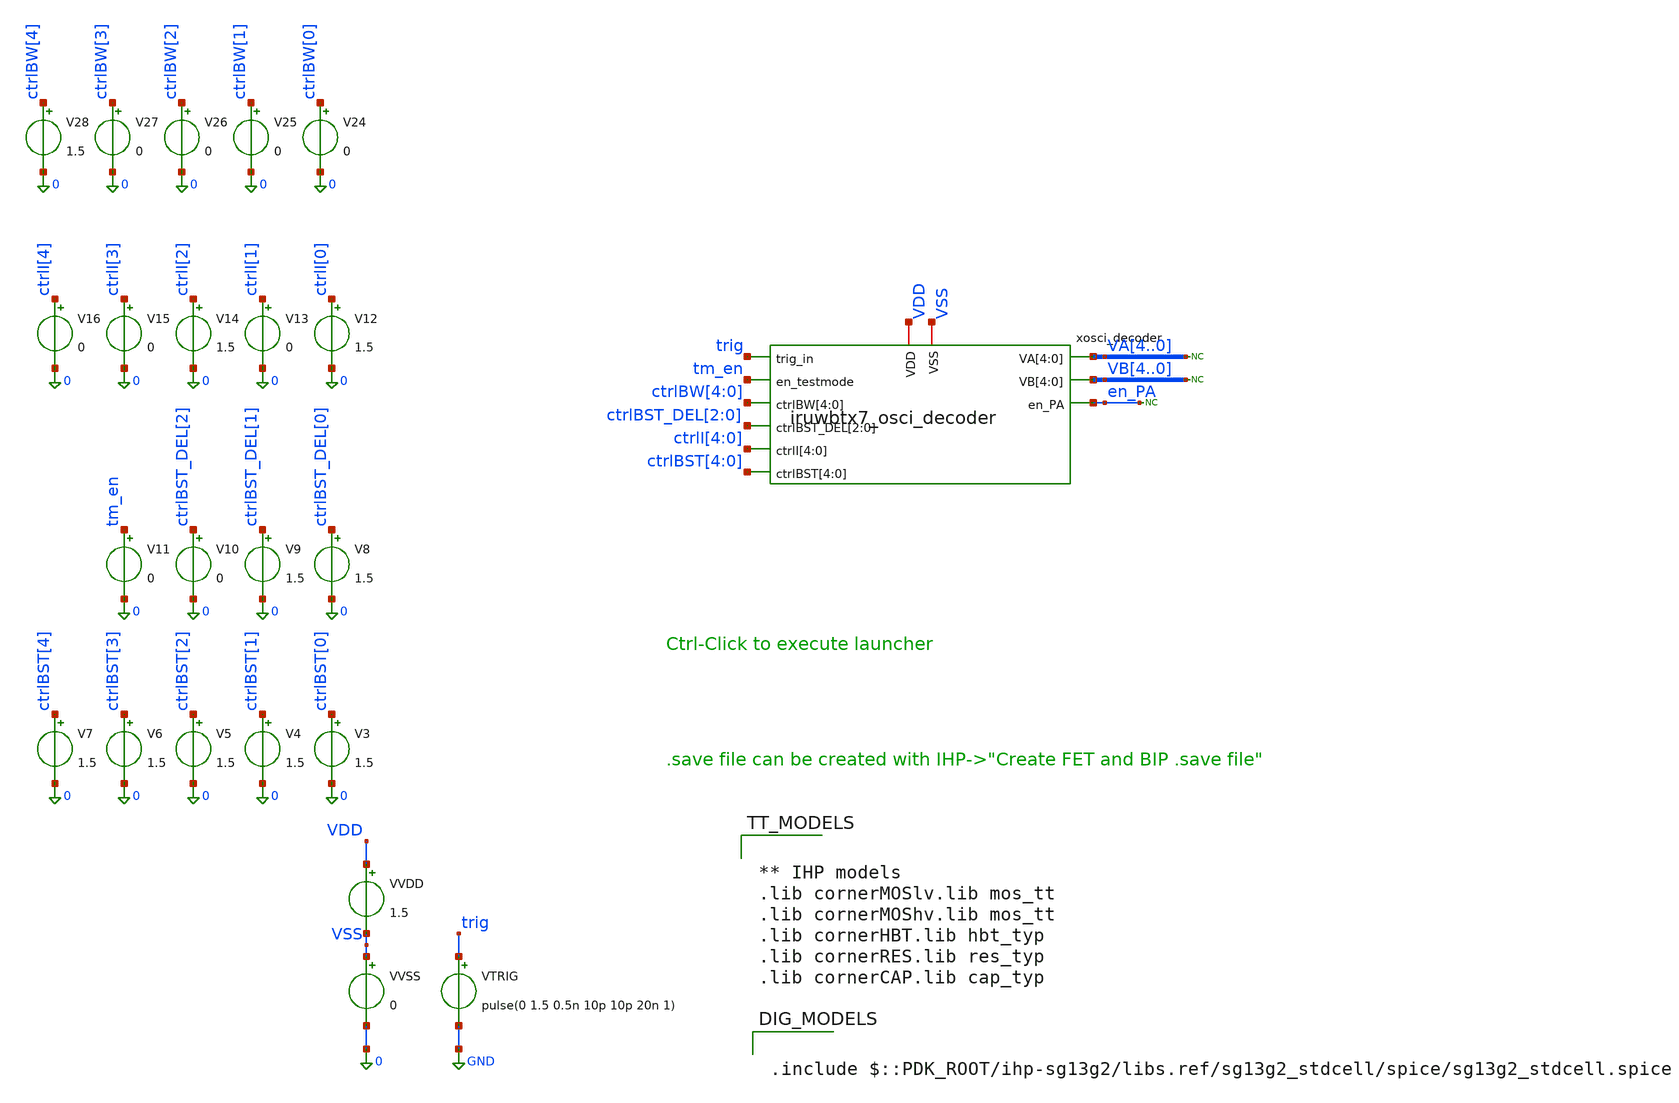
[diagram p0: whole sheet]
** sch_path: xschem/iruwbtx7_osci_decoder_tb.sch
* IHP-GmbH/IHP-Open-PDK/ihp-sg13g2/libs.tech/xschem/sg13g2_stdcells/sg13g2_inv_16.sch:
* Copyright 2023 IHP PDK Authors
* Licensed under the Apache License, Version 2.0 (the "License");
**.subckt iruwbtx7_osci_decoder_tb
VVDD VDD VSS 1.5
VVSS VSS 0 0
VTRIG trig GND pulse(0 1.5 0.5n 10p 10p 20n 1)
V3 ctrlBST[0] 0 1.5
V4 ctrlBST[1] 0 1.5
V5 ctrlBST[2] 0 1.5
V6 ctrlBST[3] 0 1.5
V7 ctrlBST[4] 0 1.5
V8 ctrlBST_DEL[0] 0 1.5
V9 ctrlBST_DEL[1] 0 1.5
V10 ctrlBST_DEL[2] 0 0
V11 tm_en 0 0
V12 ctrlI[0] 0 1.5
V13 ctrlI[1] 0 0
V14 ctrlI[2] 0 1.5
V15 ctrlI[3] 0 0
V16 ctrlI[4] 0 0
V24 ctrlBW[0] 0 0
V25 ctrlBW[1] 0 0
V26 ctrlBW[2] 0 0
V27 ctrlBW[3] 0 0
V28 ctrlBW[4] 0 1.5
xosci_decoder ctrlBW[4] ctrlBW[3] ctrlBW[2] ctrlBW[1] ctrlBW[0] ctrlBST_DEL[2] ctrlBST_DEL[1]
+ ctrlBST_DEL[0] ctrlI[4] ctrlI[3] ctrlI[2] ctrlI[1] ctrlI[0] VDD VSS ctrlBST[4] ctrlBST[3] ctrlBST[2] ctrlBST[1]
+ ctrlBST[0] tm_en VA4 VA3 VA2 VA1 VA0 trig VB4 VB3 VB2 VB1 VB0 en_PA iruwbtx7_osci_decoder
* noconn en_PA
* noconn VB[4..0]
* noconn VA[4..0]
**** begin user architecture code


** IHP models
.lib cornerMOSlv.lib mos_tt
.lib cornerMOShv.lib mos_tt
.lib cornerHBT.lib hbt_typ
.lib cornerRES.lib res_typ
.lib cornerCAP.lib cap_typ





.param temp=27
.include iruwbtx7_osci_decoder_tb.save
.options method=trap reltol=1e-4 vabstol=1e-6 iabstol=1e-12 gmin=1e-12 chgtol=1e-16 rshunt=1e12
+ trtol=1 pivotrel=1e-3 pivotabs=1e-13 noacct numdgt=7
*.options klu keepopinfo method=Gear rshunt=1e12 gmin=1e-12 reltol=100e-06 abstol=1e-12 vntol=1e-06

.control
set num_threads 1

save all
*op
*write iruwbtx7_osci_decoder_tb.raw
*set appendwrite
tran 0.5p 3.6n uic 0.5p
write iruwbtx7_osci_decoder_tb.raw
plot trig VA2 VB2 en_PA
.endc





.include $::PDK_ROOT/ihp-sg13g2/libs.ref/sg13g2_stdcell/spice/sg13g2_stdcell.spice


**** end user architecture code
**.ends

* expanding   symbol:  iruwbtx7_osci_decoder.sym # of pins=11
** sym_path: xschem/iruwbtx7_osci_decoder.sym
** sch_path: xschem/iruwbtx7_osci_decoder.sch
.subckt iruwbtx7_osci_decoder ctrlBW[4] ctrlBW[3] ctrlBW[2] ctrlBW[1] ctrlBW[0] ctrlBST_DEL[2]
+ ctrlBST_DEL[1] ctrlBST_DEL[0] ctrlI[4] ctrlI[3] ctrlI[2] ctrlI[1] ctrlI[0] VDD VSS ctrlBST[4] ctrlBST[3]
+ ctrlBST[2] ctrlBST[1] ctrlBST[0] en_testmode VA[4] VA[3] VA[2] VA[1] VA[0] trig_in VB[4] VB[3] VB[2] VB[1]
+ VB[0] en_PA
*.ipin en_testmode
*.ipin trig_in
*.ipin ctrlBW[4],ctrlBW[3],ctrlBW[2],ctrlBW[1],ctrlBW[0]
*.iopin VDD
*.iopin VSS
*.ipin ctrlBST_DEL[2],ctrlBST_DEL[1],ctrlBST_DEL[0]
*.ipin ctrlI[4],ctrlI[3],ctrlI[2],ctrlI[1],ctrlI[0]
*.ipin ctrlBST[4],ctrlBST[3],ctrlBST[2],ctrlBST[1],ctrlBST[0]
*.opin VA[4],VA[3],VA[2],VA[1],VA[0]
*.opin VB[4],VB[3],VB[2],VB[1],VB[0]
*.opin en_PA
x1 net3 en_testmode trig_in VDD VSS sg13g2_nand2_1
x2 net1 trig_in VDD VSS sg13g2_inv_1
x3 net4 net1 VDD VSS sg13g2_inv_2
x4 net2 trig_in VDD VSS sg13g2_inv_1
x5 net5 net2 VDD VSS sg13g2_inv_1
XC5 net5 net6 cap_cmim w=7.0e-6 l=7.0e-6 m=1 mm_ok=1
XM1 net6 ctrlBW[0] VSS VSS sg13_lv_nmos w=1u l=0.13u ng=1 m=1 mm_ok=1
XC1 net5 net7 cap_cmim w=7.0e-6 l=7.0e-6 m=2 mm_ok=1
XM2 net7 ctrlBW[1] VSS VSS sg13_lv_nmos w=1u l=0.13u ng=1 m=2 mm_ok=1
XC2 net5 net8 cap_cmim w=7.0e-6 l=7.0e-6 m=4 mm_ok=1
XM3 net8 ctrlBW[2] VSS VSS sg13_lv_nmos w=1u l=0.13u ng=1 m=4 mm_ok=1
XC3 net5 net9 cap_cmim w=7.0e-6 l=7.0e-6 m=8 mm_ok=1
XM4 net9 ctrlBW[3] VSS VSS sg13_lv_nmos w=1u l=0.13u ng=1 m=8 mm_ok=1
XC4 net5 net10 cap_cmim w=7.0e-6 l=7.0e-6 m=16 mm_ok=1
XM5 net10 ctrlBW[4] VSS VSS sg13_lv_nmos w=1u l=0.13u ng=1 m=16 mm_ok=1
x6 net12 net5 VDD VSS sg13g2_inv_1
x7 net11 net12 VDD VSS sg13g2_inv_2
x8 net14 net11 VDD VSS sg13g2_inv_2
x9 net13 net4 net14 VDD VSS sg13g2_nand2_2
x10 net15 net3 net13 VDD VSS sg13g2_nand2_2
x11 net24 net15 VDD VSS sg13g2_inv_2
x12 net16 trig_in VDD VSS sg13g2_inv_1
x13 net17 net16 VDD VSS sg13g2_inv_1
x14 net22 net17 VDD VSS sg13g2_inv_1
x15 net21 net22 VDD VSS sg13g2_inv_2
x16 net23 net21 VDD VSS sg13g2_inv_2
x17 net40 net4 net23 VDD VSS sg13g2_nand2_2
XM6 net17 ctrlBST_DEL[0] net18 VSS sg13_lv_nmos w=1u l=0.13u ng=1 m=1 mm_ok=1
XM7 net17 ctrlBST_DEL[1] net19 VSS sg13_lv_nmos w=1u l=0.13u ng=1 m=2 mm_ok=1
XM11 net17 ctrlBST_DEL[2] net20 VSS sg13_lv_nmos w=1u l=0.13u ng=1 m=4 mm_ok=1
XM8 VSS net18 VSS VSS sg13_lv_nmos w=0.6u l=1.0u ng=1 m=1 mm_ok=1
XM9 VSS net19 VSS VSS sg13_lv_nmos w=0.6u l=1.0u ng=1 m=2 mm_ok=1
XM10 VSS net20 VSS VSS sg13_lv_nmos w=0.6u l=1.0u ng=1 m=4 mm_ok=1
x18 net25 net24 VDD VSS sg13g2_inv_1
x19 net27 net25 VDD VSS sg13g2_inv_1
x20 net26 net27 VDD VSS sg13g2_inv_1
x21 net34 net26 VDD VSS sg13g2_inv_1
x22 net29 net24 VDD VSS sg13g2_inv_1
x23 net28 net29 VDD VSS sg13g2_inv_1
x24 net63 net28 VDD VSS sg13g2_inv_4
x25 net31 net34 VDD VSS sg13g2_inv_1
x26 net30 net31 VDD VSS sg13g2_inv_1
x27 net36 net30 VDD VSS sg13g2_inv_4
x28 net33 net24 VDD VSS sg13g2_inv_1
x29 net32 net33 VDD VSS sg13g2_inv_1
x30 net35 net32 VDD VSS sg13g2_inv_4
x31 net37 net40 VDD VSS sg13g2_inv_1
x32 net39 net37 VDD VSS sg13g2_inv_1
x33 net38 net39 VDD VSS sg13g2_inv_1
x34 net45 net38 VDD VSS sg13g2_inv_1
x35 net42 net45 VDD VSS sg13g2_inv_1
x36 net41 net42 VDD VSS sg13g2_inv_1
x37 net51 net41 VDD VSS sg13g2_inv_4
x38 net44 net40 VDD VSS sg13g2_inv_1
x39 net43 net44 VDD VSS sg13g2_inv_1
x40 net50 net43 VDD VSS sg13g2_inv_4
x41[4] net46[4] ctrlI[4] net35 VDD VSS sg13g2_nand2_2
x41[3] net46[3] ctrlI[3] net35 VDD VSS sg13g2_nand2_2
x41[2] net46[2] ctrlI[2] net35 VDD VSS sg13g2_nand2_2
x41[1] net46[1] ctrlI[1] net35 VDD VSS sg13g2_nand2_2
x41[0] net46[0] ctrlI[0] net35 VDD VSS sg13g2_nand2_2
x1[4] net47[4] net46[4] VDD VSS sg13g2_inv_2
x1[3] net47[3] net46[3] VDD VSS sg13g2_inv_2
x1[2] net47[2] net46[2] VDD VSS sg13g2_inv_2
x1[1] net47[1] net46[1] VDD VSS sg13g2_inv_2
x1[0] net47[0] net46[0] VDD VSS sg13g2_inv_2
x2[4] net48[4] net36 ctrlI[4] VDD VSS sg13g2_nand2_2
x2[3] net48[3] net36 ctrlI[3] VDD VSS sg13g2_nand2_2
x2[2] net48[2] net36 ctrlI[2] VDD VSS sg13g2_nand2_2
x2[1] net48[1] net36 ctrlI[1] VDD VSS sg13g2_nand2_2
x2[0] net48[0] net36 ctrlI[0] VDD VSS sg13g2_nand2_2
x3[4] net49[4] net48[4] VDD VSS sg13g2_inv_2
x3[3] net49[3] net48[3] VDD VSS sg13g2_inv_2
x3[2] net49[2] net48[2] VDD VSS sg13g2_inv_2
x3[1] net49[1] net48[1] VDD VSS sg13g2_inv_2
x3[0] net49[0] net48[0] VDD VSS sg13g2_inv_2
x4[4] net52[4] ctrlBST[4] net50 VDD VSS sg13g2_nand2_2
x4[3] net52[3] ctrlBST[3] net50 VDD VSS sg13g2_nand2_2
x4[2] net52[2] ctrlBST[2] net50 VDD VSS sg13g2_nand2_2
x4[1] net52[1] ctrlBST[1] net50 VDD VSS sg13g2_nand2_2
x4[0] net52[0] ctrlBST[0] net50 VDD VSS sg13g2_nand2_2
x5[4] net54[4] net52[4] VDD VSS sg13g2_inv_2
x5[3] net54[3] net52[3] VDD VSS sg13g2_inv_2
x5[2] net54[2] net52[2] VDD VSS sg13g2_inv_2
x5[1] net54[1] net52[1] VDD VSS sg13g2_inv_2
x5[0] net54[0] net52[0] VDD VSS sg13g2_inv_2
x6[4] net53[4] net51 ctrlBST[4] VDD VSS sg13g2_nand2_2
x6[3] net53[3] net51 ctrlBST[3] VDD VSS sg13g2_nand2_2
x6[2] net53[2] net51 ctrlBST[2] VDD VSS sg13g2_nand2_2
x6[1] net53[1] net51 ctrlBST[1] VDD VSS sg13g2_nand2_2
x6[0] net53[0] net51 ctrlBST[0] VDD VSS sg13g2_nand2_2
x7[4] net55[4] net53[4] VDD VSS sg13g2_inv_2
x7[3] net55[3] net53[3] VDD VSS sg13g2_inv_2
x7[2] net55[2] net53[2] VDD VSS sg13g2_inv_2
x7[1] net55[1] net53[1] VDD VSS sg13g2_inv_2
x7[0] net55[0] net53[0] VDD VSS sg13g2_inv_2
x8[4] net56[4] net54[4] net47[4] VDD VSS sg13g2_nor2_2
x8[3] net56[3] net54[3] net47[3] VDD VSS sg13g2_nor2_2
x8[2] net56[2] net54[2] net47[2] VDD VSS sg13g2_nor2_2
x8[1] net56[1] net54[1] net47[1] VDD VSS sg13g2_nor2_2
x8[0] net56[0] net54[0] net47[0] VDD VSS sg13g2_nor2_2
x42[4] net59[4] net49[4] net55[4] VDD VSS sg13g2_nor2_2
x42[3] net59[3] net49[3] net55[3] VDD VSS sg13g2_nor2_2
x42[2] net59[2] net49[2] net55[2] VDD VSS sg13g2_nor2_2
x42[1] net59[1] net49[1] net55[1] VDD VSS sg13g2_nor2_2
x42[0] net59[0] net49[0] net55[0] VDD VSS sg13g2_nor2_2
x9[4] net57[4] net56[4] VDD VSS sg13g2_inv_4
x9[3] net57[3] net56[3] VDD VSS sg13g2_inv_4
x9[2] net57[2] net56[2] VDD VSS sg13g2_inv_4
x9[1] net57[1] net56[1] VDD VSS sg13g2_inv_4
x9[0] net57[0] net56[0] VDD VSS sg13g2_inv_4
x10[4] net58[4] net57[4] VDD VSS sg13g2_inv_8
x10[3] net58[3] net57[3] VDD VSS sg13g2_inv_8
x10[2] net58[2] net57[2] VDD VSS sg13g2_inv_8
x10[1] net58[1] net57[1] VDD VSS sg13g2_inv_8
x10[0] net58[0] net57[0] VDD VSS sg13g2_inv_8
x11[4] VA[4] net58[4] VDD VSS sg13g2_inv_16
x11[3] VA[3] net58[3] VDD VSS sg13g2_inv_16
x11[2] VA[2] net58[2] VDD VSS sg13g2_inv_16
x11[1] VA[1] net58[1] VDD VSS sg13g2_inv_16
x11[0] VA[0] net58[0] VDD VSS sg13g2_inv_16
x12[4] net60[4] net59[4] VDD VSS sg13g2_inv_4
x12[3] net60[3] net59[3] VDD VSS sg13g2_inv_4
x12[2] net60[2] net59[2] VDD VSS sg13g2_inv_4
x12[1] net60[1] net59[1] VDD VSS sg13g2_inv_4
x12[0] net60[0] net59[0] VDD VSS sg13g2_inv_4
x13[4] net61[4] net60[4] VDD VSS sg13g2_inv_8
x13[3] net61[3] net60[3] VDD VSS sg13g2_inv_8
x13[2] net61[2] net60[2] VDD VSS sg13g2_inv_8
x13[1] net61[1] net60[1] VDD VSS sg13g2_inv_8
x13[0] net61[0] net60[0] VDD VSS sg13g2_inv_8
x14[4] VB[4] net61[4] VDD VSS sg13g2_inv_16
x14[3] VB[3] net61[3] VDD VSS sg13g2_inv_16
x14[2] VB[2] net61[2] VDD VSS sg13g2_inv_16
x14[1] VB[1] net61[1] VDD VSS sg13g2_inv_16
x14[0] VB[0] net61[0] VDD VSS sg13g2_inv_16
x15[4] net62[4] net63 VDD VSS sg13g2_inv_8
x15[3] net62[3] net63 VDD VSS sg13g2_inv_8
x15[2] net62[2] net63 VDD VSS sg13g2_inv_8
x15[1] net62[1] net63 VDD VSS sg13g2_inv_8
x15[0] net62[0] net63 VDD VSS sg13g2_inv_8
x16[4] en_PA net62[4] VDD VSS sg13g2_inv_16
x16[3] en_PA net62[3] VDD VSS sg13g2_inv_16
x16[2] en_PA net62[2] VDD VSS sg13g2_inv_16
x16[1] en_PA net62[1] VDD VSS sg13g2_inv_16
x16[0] en_PA net62[0] VDD VSS sg13g2_inv_16
* noconn VDD
.ends


* expanding   symbol:  sg13g2_nand2_1.sym # of pins=3
** sym_path: sg13g2_nand2_1.sym
** sch_path: sg13g2_nand2_1.sch
.subckt sg13g2_nand2_1 Y A B VDD VSS
*.iopin VDD
*.iopin VSS
*.ipin A
*.ipin B
*.opin Y
XM1 Y A net1 VSS sg13_lv_nmos w=740.00n l=130.00n ng=1 m=1 mm_ok=1
XM2 net1 B VSS VSS sg13_lv_nmos w=740.00n l=130.00n ng=1 m=1 mm_ok=1
XM3 Y A VDD VDD sg13_lv_pmos w=1.12u l=130.00n ng=1 m=1 mm_ok=1
XM4 Y B VDD VDD sg13_lv_pmos w=1.12u l=130.00n ng=1 m=1 mm_ok=1
.ends


* expanding   symbol:  sg13g2_inv_1.sym # of pins=2
** sym_path: sg13g2_inv_1.sym
** sch_path: sg13g2_inv_1.sch
.subckt sg13g2_inv_1 Y A VDD VSS
*.opin Y
*.ipin A
*.iopin VDD
*.iopin VSS
XM1 Y A VSS VSS sg13_lv_nmos w=740.00n l=130.00n ng=1 m=1 mm_ok=1
XM2 Y A VDD VDD sg13_lv_pmos w=1.12u l=130.00n ng=1 m=1 mm_ok=1
.ends


* expanding   symbol:  sg13g2_inv_2.sym # of pins=2
** sym_path: sg13g2_inv_2.sym
** sch_path: sg13g2_inv_2.sch
.subckt sg13g2_inv_2 Y A VDD VSS
*.opin Y
*.ipin A
*.iopin VDD
*.iopin VSS
XM1 Y A VSS VSS sg13_lv_nmos w=1.48u l=130.00n ng=2 m=1 mm_ok=1
XM2 Y A VDD VDD sg13_lv_pmos w=2.24u l=130.00n ng=2 m=1 mm_ok=1
.ends


* expanding   symbol:  sg13g2_nand2_2.sym # of pins=3
** sym_path: sg13g2_nand2_2.sym
** sch_path: sg13g2_nand2_2.sch
.subckt sg13g2_nand2_2 Y A B VDD VSS
*.iopin VDD
*.iopin VSS
*.opin Y
*.ipin B
*.ipin A
XM1 Y A net1 VSS sg13_lv_nmos w=1.44u l=130.00n ng=2 m=1 mm_ok=1
XM2 net1 B VSS VSS sg13_lv_nmos w=1.44u l=130.00n ng=2 m=1 mm_ok=1
XM3 Y A VDD VDD sg13_lv_pmos w=2.24u l=130.00n ng=2 m=1 mm_ok=1
XM4 Y B VDD VDD sg13_lv_pmos w=2.24u l=130.00n ng=2 m=1 mm_ok=1
.ends


* expanding   symbol:  sg13g2_inv_4.sym # of pins=2
** sym_path: sg13g2_inv_4.sym
** sch_path: sg13g2_inv_4.sch
.subckt sg13g2_inv_4 Y A VDD VSS
*.ipin A
*.opin Y
*.iopin VDD
*.iopin VSS
XM1 Y A VSS VSS sg13_lv_nmos w=2.96u l=130.00n ng=4 m=1 mm_ok=1
XM2 Y A VDD VDD sg13_lv_pmos w=4.48u l=130.00n ng=4 m=1 mm_ok=1
.ends


* expanding   symbol:  sg13g2_nor2_2.sym # of pins=3
** sym_path: sg13g2_nor2_2.sym
** sch_path: sg13g2_nor2_2.sch
.subckt sg13g2_nor2_2 Y A B VDD VSS
*.opin Y
*.ipin B
*.ipin A
*.iopin VDD
*.iopin VSS
XM1 Y A VSS VSS sg13_lv_nmos w=1.48u l=130.00n ng=2 m=1 mm_ok=1
XM2 Y B VSS VSS sg13_lv_nmos w=1.48u l=130.00n ng=2 m=1 mm_ok=1
XM3 net1 A VDD VDD sg13_lv_pmos w=2.24u l=130.00n ng=2 m=1 mm_ok=1
XM4 Y B net1 VDD sg13_lv_pmos w=2.24u l=130.00n ng=2 m=1 mm_ok=1
.ends


* expanding   symbol:  sg13g2_inv_8.sym # of pins=2
** sym_path: sg13g2_inv_8.sym
** sch_path: sg13g2_inv_8.sch
.subckt sg13g2_inv_8 Y A VDD VSS
*.opin Y
*.ipin A
*.iopin VDD
*.iopin VSS
XM1 Y A VSS VSS sg13_lv_nmos w=5.92u l=130.00n ng=8 m=1 mm_ok=1
XM2 Y A VDD VDD sg13_lv_pmos w=8.96u l=130.00n ng=8 m=1 mm_ok=1
.ends


* expanding   symbol:  sg13g2_inv_16.sym # of pins=2
** sym_path: sg13g2_inv_16.sym
** sch_path: sg13g2_inv_16.sch
.subckt sg13g2_inv_16 Y A VDD VSS
*.opin Y
*.iopin VSS
*.ipin A
*.iopin VDD
XM1 Y A VSS VSS sg13_lv_nmos w=11.84u l=130.00n ng=16 m=1 mm_ok=1
XM2 Y A VDD VDD sg13_lv_pmos w=17.92u l=130.00n ng=16 m=1 mm_ok=1
.ends

.GLOBAL GND
.end
